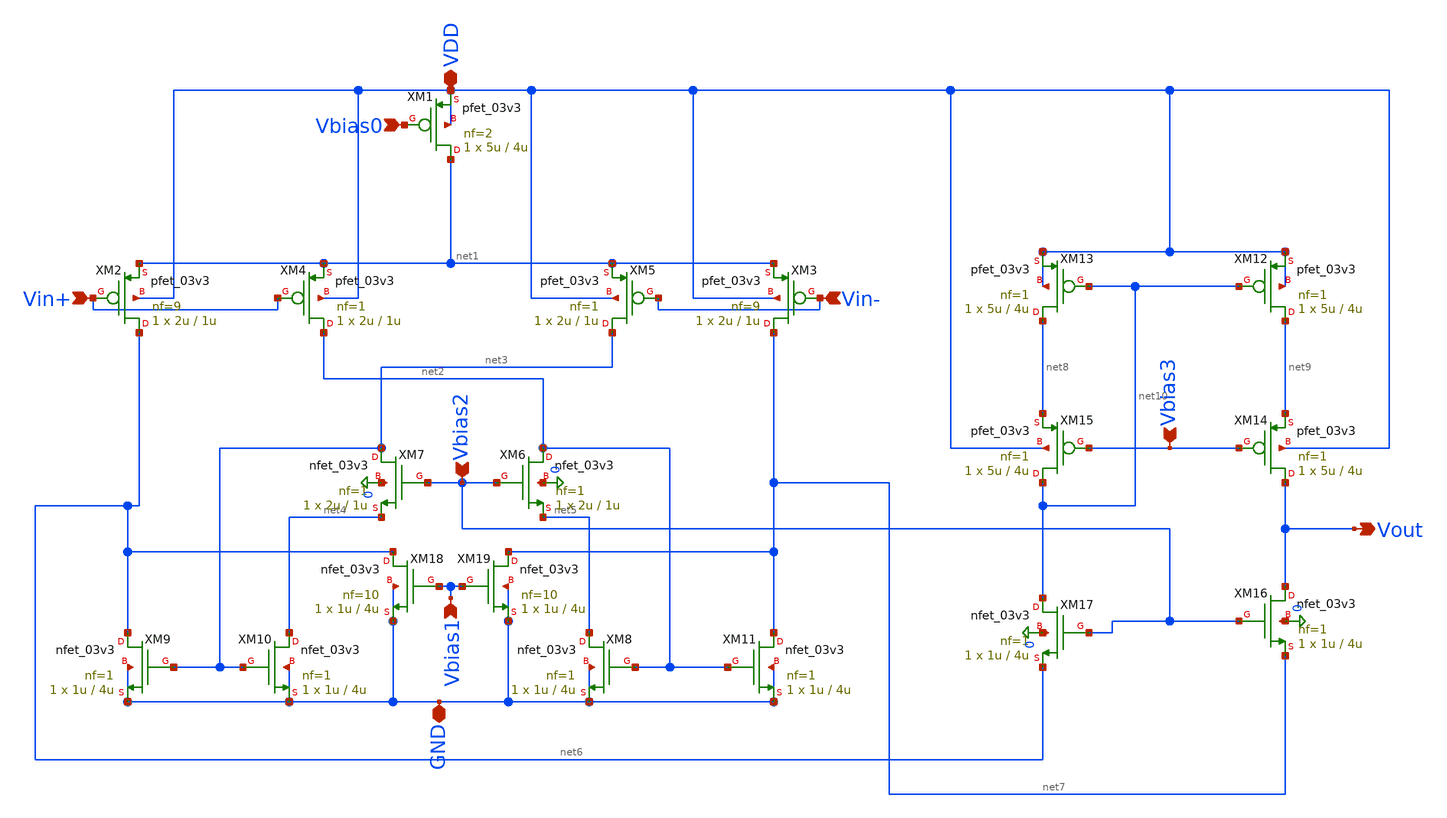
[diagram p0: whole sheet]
** sch_path: analog/B04_folded_cascode_OTA.sch
**.subckt B04_folded_cascode_OTA VDD Vbias0 Vin+ Vin- Vout Vbias3 Vbias2 GND Vbias1
*.iopin VDD
*.ipin Vbias0
*.ipin Vin+
*.ipin Vin-
*.opin Vout
*.ipin Vbias3
*.ipin Vbias2
*.iopin GND
*.ipin Vbias1
XM1 net1 Vbias0 VDD VDD pfet_03v3 L=4u W=5u nf=2 ad='int((nf+1)/2) * W/nf * 0.18u' as='int((nf+2)/2) * W/nf * 0.18u'
+ pd='2*int((nf+1)/2) * (W/nf + 0.18u)' ps='2*int((nf+2)/2) * (W/nf + 0.18u)' nrd='0.18u / W' nrs='0.18u / W'
+ sa=0 sb=0 sd=0 m=1
XM2 net6 Vin+ net1 VDD pfet_03v3 L=1u W=2u nf=9 ad='int((nf+1)/2) * W/nf * 0.18u' as='int((nf+2)/2) * W/nf * 0.18u'
+ pd='2*int((nf+1)/2) * (W/nf + 0.18u)' ps='2*int((nf+2)/2) * (W/nf + 0.18u)' nrd='0.18u / W' nrs='0.18u / W'
+ sa=0 sb=0 sd=0 m=1
XM3 net7 Vin- net1 VDD pfet_03v3 L=1u W=2u nf=9 ad='int((nf+1)/2) * W/nf * 0.18u' as='int((nf+2)/2) * W/nf * 0.18u'
+ pd='2*int((nf+1)/2) * (W/nf + 0.18u)' ps='2*int((nf+2)/2) * (W/nf + 0.18u)' nrd='0.18u / W' nrs='0.18u / W'
+ sa=0 sb=0 sd=0 m=1
XM4 net2 Vin+ net1 VDD pfet_03v3 L=1u W=2u nf=1 ad='int((nf+1)/2) * W/nf * 0.18u' as='int((nf+2)/2) * W/nf * 0.18u'
+ pd='2*int((nf+1)/2) * (W/nf + 0.18u)' ps='2*int((nf+2)/2) * (W/nf + 0.18u)' nrd='0.18u / W' nrs='0.18u / W'
+ sa=0 sb=0 sd=0 m=1
XM5 net3 Vin- net1 VDD pfet_03v3 L=1u W=2u nf=1 ad='int((nf+1)/2) * W/nf * 0.18u' as='int((nf+2)/2) * W/nf * 0.18u'
+ pd='2*int((nf+1)/2) * (W/nf + 0.18u)' ps='2*int((nf+2)/2) * (W/nf + 0.18u)' nrd='0.18u / W' nrs='0.18u / W'
+ sa=0 sb=0 sd=0 m=1
XM6 net2 Vbias2 net5 0 nfet_03v3 L=1u W=2u nf=1 ad='int((nf+1)/2) * W/nf * 0.18u' as='int((nf+2)/2) * W/nf * 0.18u'
+ pd='2*int((nf+1)/2) * (W/nf + 0.18u)' ps='2*int((nf+2)/2) * (W/nf + 0.18u)' nrd='0.18u / W' nrs='0.18u / W'
+ sa=0 sb=0 sd=0 m=1
XM7 net3 Vbias2 net4 0 nfet_03v3 L=1u W=2u nf=1 ad='int((nf+1)/2) * W/nf * 0.18u' as='int((nf+2)/2) * W/nf * 0.18u'
+ pd='2*int((nf+1)/2) * (W/nf + 0.18u)' ps='2*int((nf+2)/2) * (W/nf + 0.18u)' nrd='0.18u / W' nrs='0.18u / W'
+ sa=0 sb=0 sd=0 m=1
XM8 net5 net2 GND GND nfet_03v3 L=4u W=1u nf=1 ad='int((nf+1)/2) * W/nf * 0.18u' as='int((nf+2)/2) * W/nf * 0.18u'
+ pd='2*int((nf+1)/2) * (W/nf + 0.18u)' ps='2*int((nf+2)/2) * (W/nf + 0.18u)' nrd='0.18u / W' nrs='0.18u / W'
+ sa=0 sb=0 sd=0 m=1
XM9 net6 net3 GND GND nfet_03v3 L=4u W=1u nf=1 ad='int((nf+1)/2) * W/nf * 0.18u' as='int((nf+2)/2) * W/nf * 0.18u'
+ pd='2*int((nf+1)/2) * (W/nf + 0.18u)' ps='2*int((nf+2)/2) * (W/nf + 0.18u)' nrd='0.18u / W' nrs='0.18u / W'
+ sa=0 sb=0 sd=0 m=1
XM10 net4 net3 GND GND nfet_03v3 L=4u W=1u nf=1 ad='int((nf+1)/2) * W/nf * 0.18u' as='int((nf+2)/2) * W/nf * 0.18u'
+ pd='2*int((nf+1)/2) * (W/nf + 0.18u)' ps='2*int((nf+2)/2) * (W/nf + 0.18u)' nrd='0.18u / W' nrs='0.18u / W'
+ sa=0 sb=0 sd=0 m=1
XM11 net7 net2 GND GND nfet_03v3 L=4u W=1u nf=1 ad='int((nf+1)/2) * W/nf * 0.18u' as='int((nf+2)/2) * W/nf * 0.18u'
+ pd='2*int((nf+1)/2) * (W/nf + 0.18u)' ps='2*int((nf+2)/2) * (W/nf + 0.18u)' nrd='0.18u / W' nrs='0.18u / W'
+ sa=0 sb=0 sd=0 m=1
XM12 net9 net10 VDD VDD pfet_03v3 L=4u W=5u nf=1 ad='int((nf+1)/2) * W/nf * 0.18u' as='int((nf+2)/2) * W/nf * 0.18u'
+ pd='2*int((nf+1)/2) * (W/nf + 0.18u)' ps='2*int((nf+2)/2) * (W/nf + 0.18u)' nrd='0.18u / W' nrs='0.18u / W'
+ sa=0 sb=0 sd=0 m=1
XM13 net8 net10 VDD VDD pfet_03v3 L=4u W=5u nf=1 ad='int((nf+1)/2) * W/nf * 0.18u' as='int((nf+2)/2) * W/nf * 0.18u'
+ pd='2*int((nf+1)/2) * (W/nf + 0.18u)' ps='2*int((nf+2)/2) * (W/nf + 0.18u)' nrd='0.18u / W' nrs='0.18u / W'
+ sa=0 sb=0 sd=0 m=1
XM14 Vout Vbias3 net9 VDD pfet_03v3 L=4u W=5u nf=1 ad='int((nf+1)/2) * W/nf * 0.18u' as='int((nf+2)/2) * W/nf * 0.18u'
+ pd='2*int((nf+1)/2) * (W/nf + 0.18u)' ps='2*int((nf+2)/2) * (W/nf + 0.18u)' nrd='0.18u / W' nrs='0.18u / W'
+ sa=0 sb=0 sd=0 m=1
XM15 net10 Vbias3 net8 VDD pfet_03v3 L=4u W=5u nf=1 ad='int((nf+1)/2) * W/nf * 0.18u' as='int((nf+2)/2) * W/nf * 0.18u'
+ pd='2*int((nf+1)/2) * (W/nf + 0.18u)' ps='2*int((nf+2)/2) * (W/nf + 0.18u)' nrd='0.18u / W' nrs='0.18u / W'
+ sa=0 sb=0 sd=0 m=1
XM16 Vout Vbias2 net7 0 nfet_03v3 L=4u W=1u nf=1 ad='int((nf+1)/2) * W/nf * 0.18u' as='int((nf+2)/2) * W/nf * 0.18u'
+ pd='2*int((nf+1)/2) * (W/nf + 0.18u)' ps='2*int((nf+2)/2) * (W/nf + 0.18u)' nrd='0.18u / W' nrs='0.18u / W'
+ sa=0 sb=0 sd=0 m=1
XM17 net10 Vbias2 net6 0 nfet_03v3 L=4u W=1u nf=1 ad='int((nf+1)/2) * W/nf * 0.18u' as='int((nf+2)/2) * W/nf * 0.18u'
+ pd='2*int((nf+1)/2) * (W/nf + 0.18u)' ps='2*int((nf+2)/2) * (W/nf + 0.18u)' nrd='0.18u / W' nrs='0.18u / W'
+ sa=0 sb=0 sd=0 m=1
XM18 net6 Vbias1 GND GND nfet_03v3 L=4u W=1u nf=10 ad='int((nf+1)/2) * W/nf * 0.18u' as='int((nf+2)/2) * W/nf * 0.18u'
+ pd='2*int((nf+1)/2) * (W/nf + 0.18u)' ps='2*int((nf+2)/2) * (W/nf + 0.18u)' nrd='0.18u / W' nrs='0.18u / W'
+ sa=0 sb=0 sd=0 m=1
XM19 net7 Vbias1 GND GND nfet_03v3 L=4u W=1u nf=10 ad='int((nf+1)/2) * W/nf * 0.18u' as='int((nf+2)/2) * W/nf * 0.18u'
+ pd='2*int((nf+1)/2) * (W/nf + 0.18u)' ps='2*int((nf+2)/2) * (W/nf + 0.18u)' nrd='0.18u / W' nrs='0.18u / W'
+ sa=0 sb=0 sd=0 m=1
**.ends
.end
